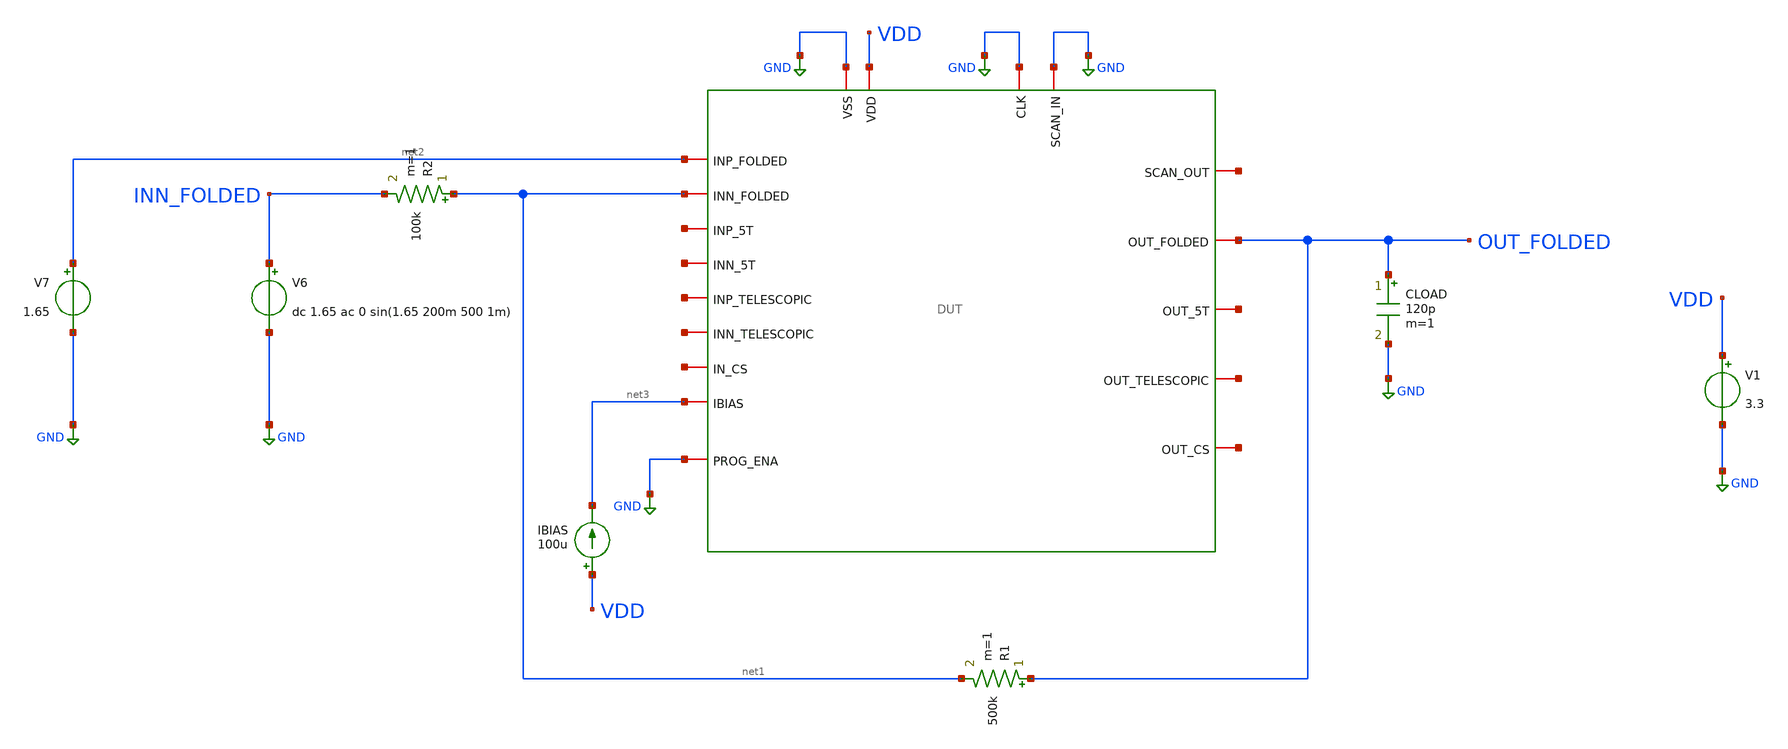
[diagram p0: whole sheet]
** sch_path: designs/libs/verification/ota_folded/default_sizing_tb.sch
**.subckt default_sizing_tb
x1 GND net4 GND GND VDD OUT_FOLDED net2 net5 net3 net1 net6 net7 net8 net9 net10 net11 net12 GND DUT
V1 VDD GND 3.3
CLOAD OUT_FOLDED GND 120p m=1
R1 OUT_FOLDED net1 500k m=1
R2 net1 INN_FOLDED 100k m=1
V6 INN_FOLDED GND dc 1.65 ac 0 sin(1.65 200m 500 1m)
V7 net2 GND 1.65
IBIAS VDD net3 100u
**** begin user architecture code

.include $::180MCU_MODELS/design.ngspice
.lib $::180MCU_MODELS/sm141064.ngspice typical



.control
tran 1u 5m
plot v(OUT_FOLDED) v(INN_FOLDED)
meas tran vout_pp pp v(out_folded) from=5m to=10m
meas tran vin_pp pp v(inn_folded) from=5m to=10m
let gain = vout_pp / vin_pp
print gain
.endc


**** end user architecture code
**.ends
.GLOBAL GND
.end
